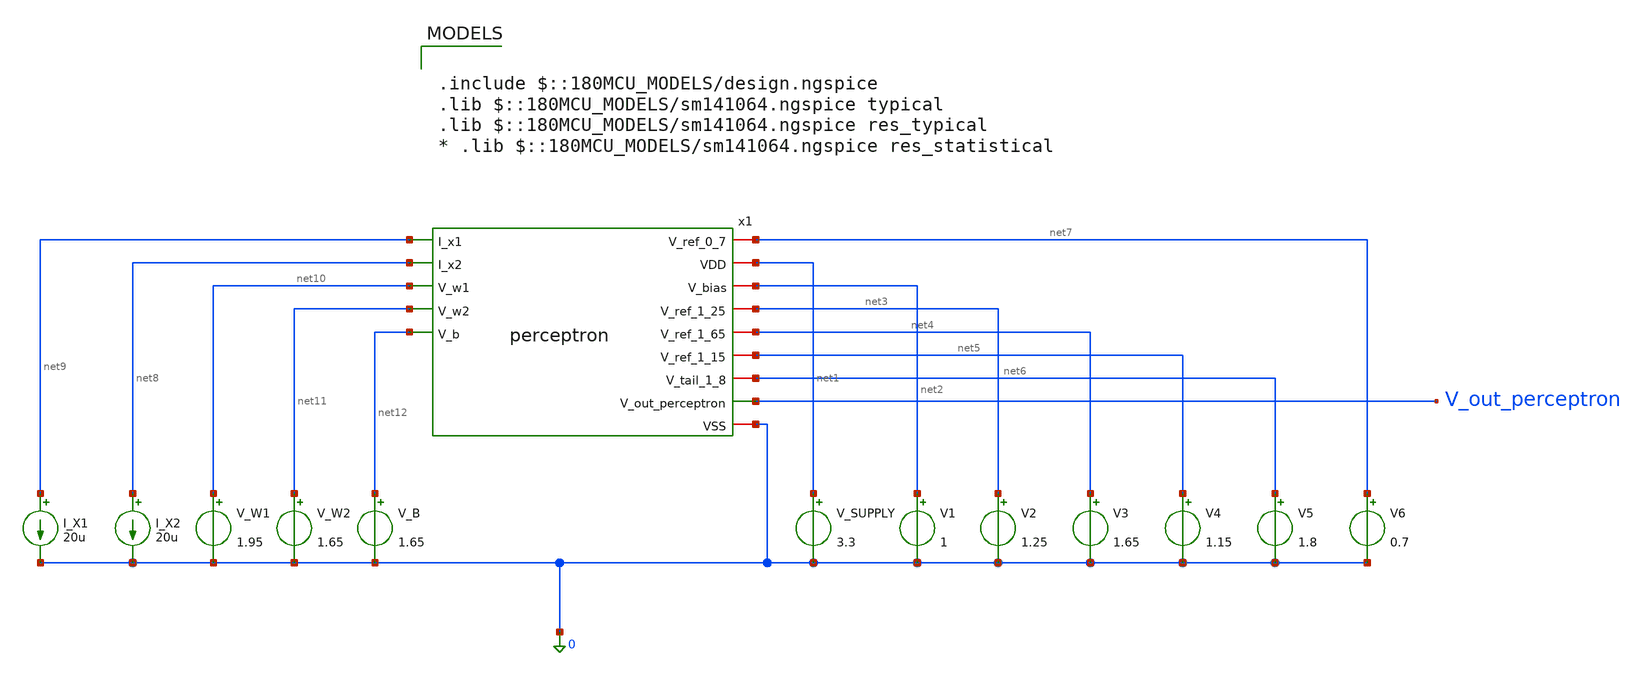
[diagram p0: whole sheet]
** sch_path: schematics/tb_perceptron.sch
**.subckt tb_perceptron
x1 net7 net1 net2 net3 net4 net5 net6 net9 net8 V_out_perceptron net10 net11 0 net12 perceptron
V_SUPPLY net1 0 3.3
V1 net2 0 1
V2 net3 0 1.25
V3 net4 0 1.65
V4 net5 0 1.15
V5 net6 0 1.8
V6 net7 0 0.7
I_X1 net9 0 20u
I_X2 net8 0 20u
V_W1 net10 0 1.95
V_W2 net11 0 1.65
V_B net12 0 1.65
**** begin user architecture code


.control
  dc I_X1 0u 50u 1u
  plot v(V_out_perceptron)
.endc



.include $::180MCU_MODELS/design.ngspice
.lib $::180MCU_MODELS/sm141064.ngspice typical
.lib $::180MCU_MODELS/sm141064.ngspice res_typical
* .lib $::180MCU_MODELS/sm141064.ngspice res_statistical

**** end user architecture code
**.ends

* expanding   symbol:  analog-perceptron-gf180mcu/schematics/perceptron.sym # of pins=14
** sym_path: schematics/perceptron.sym
** sch_path: schematics/perceptron.sch
.subckt perceptron V_ref_0_7 VDD V_bias V_ref_1_25 V_ref_1_65 V_ref_1_15 V_tail_1_8 I_x1 I_x2
+ V_out_perceptron V_w1 V_w2 VSS V_b
*.iopin VDD
*.iopin VSS
*.iopin V_bias
*.ipin I_x1
*.ipin I_x2
*.iopin V_ref_1_25
*.iopin V_ref_1_15
*.iopin V_ref_1_65
*.iopin V_tail_1_8
*.ipin V_w1
*.ipin V_w2
*.ipin V_b
*.iopin V_ref_0_7
*.opin V_out_perceptron
x1 V_ref_1_25 net1 V_bias I_x1 VSS cg_amp_tia
x2 V_ref_1_25 net2 V_bias I_x2 VSS cg_amp_tia
x_g1 net3 net4 V_w1 V_ref_1_65 net1 V_ref_1_15 V_tail_1_8 VSS gilbert_multiplier_current
x_g2 net3 net4 V_w2 V_ref_1_65 net2 V_ref_1_15 V_tail_1_8 VSS gilbert_multiplier_current
x_g3 net3 net4 V_b V_ref_1_65 V_ref_1_25 V_ref_1_15 V_tail_1_8 VSS gilbert_multiplier_current
x_tanh VDD V_ref_1_65 V_out_perceptron net3 net4 V_ref_0_7 VSS tanh_ota
XR1 net3 VDD VSS ppolyf_u r_width=1e-6 r_length=7e-6 m=1
XR2 net4 VDD VSS ppolyf_u r_width=1e-6 r_length=7e-6 m=1
.ends


* expanding   symbol:  analog-perceptron-gf180mcu/schematics/cg_amp_tia.sym # of pins=5
** sym_path: schematics/cg_amp_tia.sym
** sch_path: schematics/cg_amp_tia.sch
.subckt cg_amp_tia V_ref V_out V_bias I_in VSS
*.iopin V_ref
*.iopin VSS
*.ipin I_in
*.ipin V_bias
*.opin V_out
XM1 V_out V_bias I_in VSS nfet_03v3 L=0.5u W=10u nf=1 ad='int((nf+1)/2) * W/nf * 0.18u' as='int((nf+2)/2) * W/nf * 0.18u'
+ pd='2*int((nf+1)/2) * (W/nf + 0.18u)' ps='2*int((nf+2)/2) * (W/nf + 0.18u)' nrd='0.18u / W' nrs='0.18u / W'
+ sa=0 sb=0 sd=0 m=1
XR1 V_out V_ref VSS ppolyf_u r_width=1e-6 r_length=7e-6 m=1
.ends


* expanding   symbol:  analog-perceptron-gf180mcu/schematics/gilbert_multiplier_current.sym # of
*+ pins=8
** sym_path: schematics/gilbert_multiplier_current.sym
** sch_path: schematics/gilbert_multiplier_current.sch
.subckt gilbert_multiplier_current I_o_p I_o_n V_w_p V_w_n V_x_p V_x_n V_tail VSS
*.ipin V_x_p
*.ipin V_x_n
*.ipin V_tail
*.iopin VSS
*.ipin V_w_p
*.ipin V_w_n
*.opin I_o_n
*.opin I_o_p
XM1 net1 V_x_p net3 VSS nfet_03v3 L=0.5u W=10u nf=1 ad='int((nf+1)/2) * W/nf * 0.18u' as='int((nf+2)/2) * W/nf * 0.18u'
+ pd='2*int((nf+1)/2) * (W/nf + 0.18u)' ps='2*int((nf+2)/2) * (W/nf + 0.18u)' nrd='0.18u / W' nrs='0.18u / W'
+ sa=0 sb=0 sd=0 m=1
XM2 net2 V_x_n net4 VSS nfet_03v3 L=0.5u W=10u nf=1 ad='int((nf+1)/2) * W/nf * 0.18u' as='int((nf+2)/2) * W/nf * 0.18u'
+ pd='2*int((nf+1)/2) * (W/nf + 0.18u)' ps='2*int((nf+2)/2) * (W/nf + 0.18u)' nrd='0.18u / W' nrs='0.18u / W'
+ sa=0 sb=0 sd=0 m=1
XM3 I_o_n V_w_p net1 VSS nfet_03v3 L=0.5u W=10u nf=1 ad='int((nf+1)/2) * W/nf * 0.18u' as='int((nf+2)/2) * W/nf * 0.18u'
+ pd='2*int((nf+1)/2) * (W/nf + 0.18u)' ps='2*int((nf+2)/2) * (W/nf + 0.18u)' nrd='0.18u / W' nrs='0.18u / W'
+ sa=0 sb=0 sd=0 m=1
XM4 I_o_p V_w_n net1 VSS nfet_03v3 L=0.5u W=10u nf=1 ad='int((nf+1)/2) * W/nf * 0.18u' as='int((nf+2)/2) * W/nf * 0.18u'
+ pd='2*int((nf+1)/2) * (W/nf + 0.18u)' ps='2*int((nf+2)/2) * (W/nf + 0.18u)' nrd='0.18u / W' nrs='0.18u / W'
+ sa=0 sb=0 sd=0 m=1
XM5 I_o_n V_w_n net2 VSS nfet_03v3 L=0.5u W=10u nf=1 ad='int((nf+1)/2) * W/nf * 0.18u' as='int((nf+2)/2) * W/nf * 0.18u'
+ pd='2*int((nf+1)/2) * (W/nf + 0.18u)' ps='2*int((nf+2)/2) * (W/nf + 0.18u)' nrd='0.18u / W' nrs='0.18u / W'
+ sa=0 sb=0 sd=0 m=1
XM6 I_o_p V_w_p net2 VSS nfet_03v3 L=0.5u W=10u nf=1 ad='int((nf+1)/2) * W/nf * 0.18u' as='int((nf+2)/2) * W/nf * 0.18u'
+ pd='2*int((nf+1)/2) * (W/nf + 0.18u)' ps='2*int((nf+2)/2) * (W/nf + 0.18u)' nrd='0.18u / W' nrs='0.18u / W'
+ sa=0 sb=0 sd=0 m=1
XM7 net3 V_tail VSS VSS nfet_03v3 L=1u W=5u nf=1 ad='int((nf+1)/2) * W/nf * 0.18u' as='int((nf+2)/2) * W/nf * 0.18u'
+ pd='2*int((nf+1)/2) * (W/nf + 0.18u)' ps='2*int((nf+2)/2) * (W/nf + 0.18u)' nrd='0.18u / W' nrs='0.18u / W'
+ sa=0 sb=0 sd=0 m=1
XM8 net4 V_tail VSS VSS nfet_03v3 L=1u W=5u nf=1 ad='int((nf+1)/2) * W/nf * 0.18u' as='int((nf+2)/2) * W/nf * 0.18u'
+ pd='2*int((nf+1)/2) * (W/nf + 0.18u)' ps='2*int((nf+2)/2) * (W/nf + 0.18u)' nrd='0.18u / W' nrs='0.18u / W'
+ sa=0 sb=0 sd=0 m=1
XR1 net3 net4 VSS ppolyf_u r_width=1e-6 r_length=40e-6 m=1
.ends


* expanding   symbol:  analog-perceptron-gf180mcu/schematics/tanh_ota.sym # of pins=7
** sym_path: schematics/tanh_ota.sym
** sch_path: schematics/tanh_ota.sch
.subckt tanh_ota VDD V_ref V_out V_in_p V_in_n V_bias VSS
*.iopin VDD
*.iopin VSS
*.ipin V_in_p
*.ipin V_in_n
*.ipin V_bias
*.opin V_out
*.iopin V_ref
XM1 net2 V_in_p net1 VSS nfet_03v3 L=0.5u W=10u nf=1 ad='int((nf+1)/2) * W/nf * 0.18u' as='int((nf+2)/2) * W/nf * 0.18u'
+ pd='2*int((nf+1)/2) * (W/nf + 0.18u)' ps='2*int((nf+2)/2) * (W/nf + 0.18u)' nrd='0.18u / W' nrs='0.18u / W'
+ sa=0 sb=0 sd=0 m=1
XM2 V_out V_in_n net1 VSS nfet_03v3 L=0.5u W=10u nf=1 ad='int((nf+1)/2) * W/nf * 0.18u' as='int((nf+2)/2) * W/nf * 0.18u'
+ pd='2*int((nf+1)/2) * (W/nf + 0.18u)' ps='2*int((nf+2)/2) * (W/nf + 0.18u)' nrd='0.18u / W' nrs='0.18u / W'
+ sa=0 sb=0 sd=0 m=1
XM3 net1 V_bias VSS VSS nfet_03v3 L=0.5u W=10u nf=1 ad='int((nf+1)/2) * W/nf * 0.18u' as='int((nf+2)/2) * W/nf * 0.18u'
+ pd='2*int((nf+1)/2) * (W/nf + 0.18u)' ps='2*int((nf+2)/2) * (W/nf + 0.18u)' nrd='0.18u / W' nrs='0.18u / W'
+ sa=0 sb=0 sd=0 m=1
XM4 net2 net2 VDD VDD pfet_03v3 L=0.5u W=20u nf=1 ad='int((nf+1)/2) * W/nf * 0.18u' as='int((nf+2)/2) * W/nf * 0.18u'
+ pd='2*int((nf+1)/2) * (W/nf + 0.18u)' ps='2*int((nf+2)/2) * (W/nf + 0.18u)' nrd='0.18u / W' nrs='0.18u / W'
+ sa=0 sb=0 sd=0 m=1
XM5 V_out net2 VDD VDD pfet_03v3 L=0.5u W=20u nf=1 ad='int((nf+1)/2) * W/nf * 0.18u' as='int((nf+2)/2) * W/nf * 0.18u'
+ pd='2*int((nf+1)/2) * (W/nf + 0.18u)' ps='2*int((nf+2)/2) * (W/nf + 0.18u)' nrd='0.18u / W' nrs='0.18u / W'
+ sa=0 sb=0 sd=0 m=1
XR1 V_out V_ref VSS ppolyf_u r_width=1e-6 r_length=64e-6 m=1
.ends

.end
